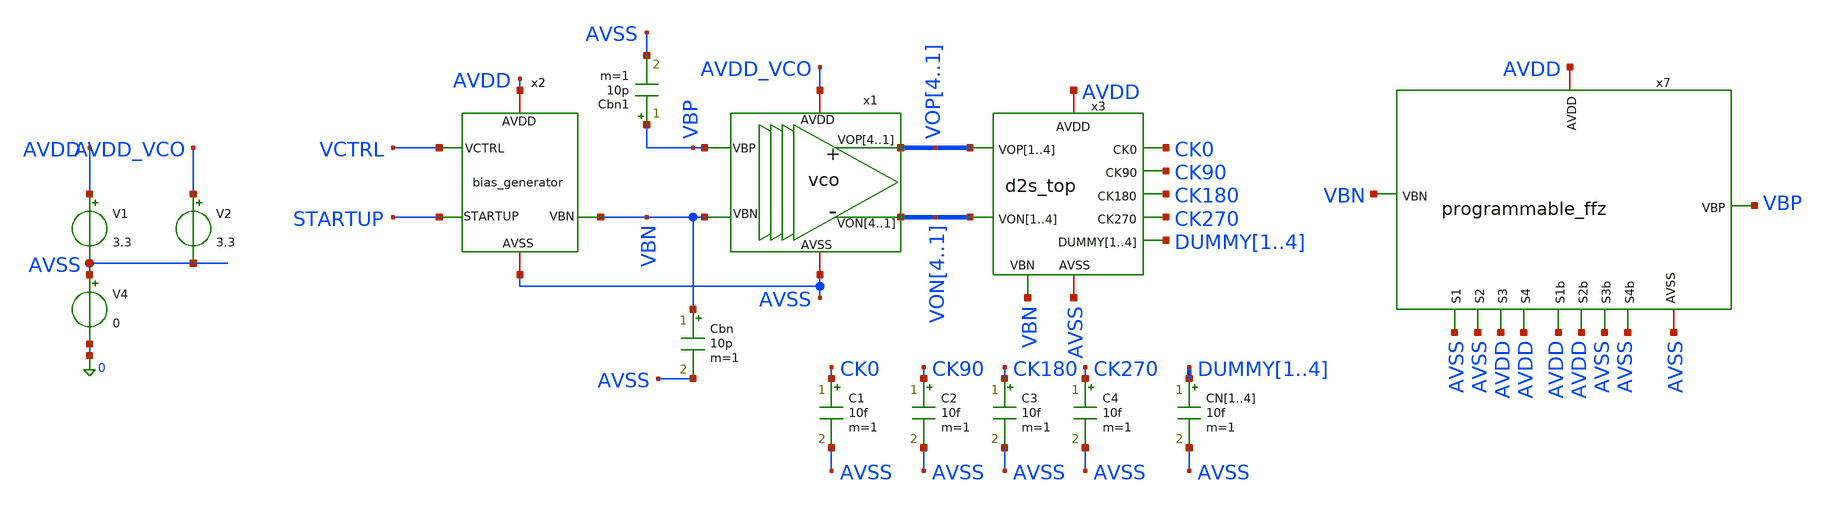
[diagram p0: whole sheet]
** sch_path: designs/libs/tb_analog/tb_quadrature_vco/tb_quadrature_vco.sch
**.subckt tb_quadrature_vco
x1 VOP4 VOP3 VOP2 VOP1 VON4 VON3 VON2 VON1 AVDD_VCO AVSS VBP VBN vco
V1 AVDD AVSS 3.3
V4 AVSS 0 0
CN1 DUMMY1 AVSS 10f m=1
CN2 DUMMY2 AVSS 10f m=1
CN3 DUMMY3 AVSS 10f m=1
CN4 DUMMY4 AVSS 10f m=1
x2 VCTRL AVDD STARTUP AVSS VBN bias_generator
Cbn VBN AVSS 10p m=1
V2 AVDD_VCO AVSS 3.3
Cbn1 VBP AVSS 10p m=1
x7 VBP AVSS AVDD VBN AVDD AVSS AVDD AVSS AVSS AVDD AVSS AVDD programmable_ffz
x3 VOP4 VOP3 VOP2 VOP1 VON4 VON3 VON2 VON1 VBN DUMMY1 DUMMY2 DUMMY3 DUMMY4 CK0 CK90 CK180 CK270 AVDD
+ AVSS d2s_top
C1 CK0 AVSS 10f m=1
C2 CK90 AVSS 10f m=1
C3 CK180 AVSS 10f m=1
C4 CK270 AVSS 10f m=1
**** begin user architecture code


.param Vin=0 Vcm=2.5
.ic v(vop1)=3.3 v(von1)=0 v(startup)=0 v(vbp)=0
.param t1=1u t2=2u t3=3u t4=4u t5=5u t6=6u t7=10u t8=50u t9=500u tr=10n

.param d0=0 d1=0.35 d2=0.825 d3=1.2375 d4=1.65 d5=2.0625 d6=2.475 d7=2.6 d8=2.75

vs startup 0 pulse(0 1 100n 10n 10n 100n 100m)
vctrl vctrl 0 pwl(0 d0  t1 d0 't1+tr' d1 t2 d1 't2+tr' d2 t3 d2 't3+tr' d3 t4 d3 't4+tr' d4 t5 d4 't5+tr'
+ d5 t6 d5 't6+tr' d6 t7 d6 't7+tr' d7 t8 d7 't8+tr' d8 t9 d8 't9+tr' d0 R 0)

*vctrl vctrl 0 d8

.control
set wr_singlescale
set wr_vecnames

save v(CK0) v(CK90) v(CK180) v(CK270) v(vctrl) v(vbp) v(vbn) v(dummy1) v(dummy2) v(dummy3) v(dummy4)
+ v(VOP1) v(VOP2) v(VOP3) v(VOP4) v(VON1) v(VON2) v(VON3) v(VON4)

OP
show all

tran 1n 1.5m
*tran 10n 500u
*tran 10p 50n



*let sum = v(VOP1) + v(VON1)
*let diff = v(VOP1) - v(VON1)
*let gain = deriv(diff)
*let vcm = AVG(sum/2)


*meas tran vmax MAX v(VOP1) FROM=10n TO=20n
*meas tran vmin MIN v(VOP1) FROM=10n TO=20n
*let vswing = vmax-vmin

meas tran I_tail_avg1 AVG i(v.x1.x1.vmeas) FROM=1.01u TO=2u
meas tran I_tail_avg2 AVG i(v.x1.x1.vmeas) FROM=2.01u TO=3u
meas tran I_tail_avg3 AVG i(v.x1.x1.vmeas) FROM=3.01u TO=4u
meas tran I_tail_avg4 AVG i(v.x1.x1.vmeas) FROM=4.01u TO=5u
meas tran I_tail_avg5 AVG i(v.x1.x1.vmeas) FROM=5.01u TO=6u
meas tran I_tail_avg6 AVG i(v.x1.x1.vmeas) FROM=6.01u TO=10u
meas tran I_tail_avg7 AVG i(v.x1.x1.vmeas) FROM=10.01u TO=50u
meas tran I_tail_avg8 AVG i(v.x1.x1.vmeas) FROM=50.01u TO=500u

*meas tran I_d2s1 AVG i(v.x3.x1.vmeas) FROM=1.01u TO=2u
*meas tran I_d2s2 AVG i(v.x3.x1.vmeas) FROM=2.01u TO=3u
*meas tran I_d2s3 AVG i(v.x3.x1.vmeas) FROM=3.01u TO=4u
*meas tran I_d2s4 AVG i(v.x3.x1.vmeas) FROM=4.01u TO=5u
*meas tran I_d2s5 AVG i(v.x3.x1.vmeas) FROM=5.01u TO=6u
*meas tran I_d2s6 AVG i(v.x3.x1.vmeas) FROM=6.01u TO=10u
*meas tran I_d2s7 AVG i(v.x3.x1.vmeas) FROM=10.01u TO=50u
*meas tran I_d2s8 AVG i(v.x3.x1.vmeas) FROM=50.01u TO=500u

*meas tran I_VCO1 AVG i(V2) FROM=1.01u TO=2u
*meas tran I_VCO2 AVG i(V2) FROM=2.01u TO=3u
*meas tran I_VCO3 AVG i(V2) FROM=3.01u TO=4u
*meas tran I_VCO4 AVG i(V2) FROM=4.01u TO=5u
*meas tran I_VCO5 AVG i(V2) FROM=5.01u TO=6u
*meas tran I_VCO6 AVG i(V2) FROM=6.01u TO=10u
*meas tran I_VCO7 AVG i(V2) FROM=10.01u TO=100u
*meas tran I_VCO8 AVG i(V2) FROM=100.01u TO=1m

remzerovec
*linearize v(CK0) v(CK90) v(CK180) v(CK270)
write tb_quadrature_vco_2.raw
destroy all
exit
*wrdata
*+ /foss/designs/synchronos-chipathon-2026/designs/libs/scripts/sim_data/tb_quadrature_vco_free_running_test.txt tran.all
.endc



.include $::180MCU_MODELS/design.ngspice
.lib $::180MCU_MODELS/sm141064.ngspice typical
*.lib $::180MCU_MODELS/sm141064.ngspice SS
*.lib $::180MCU_MODELS/sm141064.ngspice FF
*.lib $::180MCU_MODELS/sm141064.ngspice SF
*.lib $::180MCU_MODELS/sm141064.ngspice FS

**** end user architecture code
**.ends
.end
